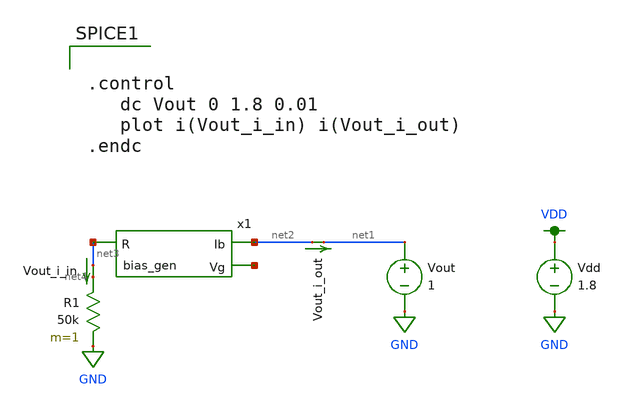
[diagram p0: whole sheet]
** sch_path: test_harness_current_mirror_complex.sch
**.subckt test_harness_current_mirror_complex
Vdd VDD GND 1.8
R1 net4 GND 50k m=1
x1 net2 net5 net3 bias_gen
Vout_i_in net3 net4 0
.save i(vout_i_in)
Vout net1 GND 1
Vout_i_out net2 net1 0
.save i(vout_i_out)
**** begin user architecture code


.control
   dc Vout 0 1.8 0.01
   plot i(Vout_i_in) i(Vout_i_out)
.endc


.option wnflag=1
.param MC_SWITCH=0.0
.lib ~/skywater/skywater-pdk/libraries/sky130_fd_pr_ngspice/latest/models/sky130.lib.spice tt

**** end user architecture code
**.ends

* expanding   symbol:  /home/madvlsi/Documents/R2R-DAC/bias_gen.sym # of pins=3
** sym_path: bias_gen.sym
** sch_path: bias_gen.sch
.subckt bias_gen Ib Vg R
*.ipin R
*.opin Ib
*.opin Vg
XM2 R net2 net2 GND sky130_fd_pr__nfet_01v8 L=4 W=96 nf=1 ad='int((nf+1)/2) * W/nf * 0.29' as='int((nf+2)/2) * W/nf * 0.29'
+ pd='2*int((nf+1)/2) * (W/nf + 0.29)' ps='2*int((nf+2)/2) * (W/nf + 0.29)' nrd='0.29 / W' nrs='0.29 / W'
+ sa=0 sb=0 sd=0 mult=1 m=1
XM3 VDD net1 net1 VDD sky130_fd_pr__pfet_01v8 L=4 W=12 nf=1 ad='int((nf+1)/2) * W/nf * 0.29' as='int((nf+2)/2) * W/nf * 0.29'
+ pd='2*int((nf+1)/2) * (W/nf + 0.29)' ps='2*int((nf+2)/2) * (W/nf + 0.29)' nrd='0.29 / W' nrs='0.29 / W'
+ sa=0 sb=0 sd=0 mult=1 m=1
XM1 VDD Vg net2 VDD sky130_fd_pr__pfet_01v8 L=4 W=12 nf=1 ad='int((nf+1)/2) * W/nf * 0.29' as='int((nf+2)/2) * W/nf * 0.29'
+ pd='2*int((nf+1)/2) * (W/nf + 0.29)' ps='2*int((nf+2)/2) * (W/nf + 0.29)' nrd='0.29 / W' nrs='0.29 / W'
+ sa=0 sb=0 sd=0 mult=1 m=1
XM4 Vg net1 VDD VDD sky130_fd_pr__pfet_01v8 L=4 W=12 nf=1 ad='int((nf+1)/2) * W/nf * 0.29' as='int((nf+2)/2) * W/nf * 0.29'
+ pd='2*int((nf+1)/2) * (W/nf + 0.29)' ps='2*int((nf+2)/2) * (W/nf + 0.29)' nrd='0.29 / W' nrs='0.29 / W'
+ sa=0 sb=0 sd=0 mult=1 m=1
XM5 net3 Vg VDD VDD sky130_fd_pr__pfet_01v8 L=4 W=12 nf=1 ad='int((nf+1)/2) * W/nf * 0.29' as='int((nf+2)/2) * W/nf * 0.29'
+ pd='2*int((nf+1)/2) * (W/nf + 0.29)' ps='2*int((nf+2)/2) * (W/nf + 0.29)' nrd='0.29 / W' nrs='0.29 / W'
+ sa=0 sb=0 sd=0 mult=1 m=1
XM7 Ib Vg VDD VDD sky130_fd_pr__pfet_01v8 L=4 W=12 nf=1 ad='int((nf+1)/2) * W/nf * 0.29' as='int((nf+2)/2) * W/nf * 0.29'
+ pd='2*int((nf+1)/2) * (W/nf + 0.29)' ps='2*int((nf+2)/2) * (W/nf + 0.29)' nrd='0.29 / W' nrs='0.29 / W'
+ sa=0 sb=0 sd=0 mult=1 m=1
XM6 net1 net2 GND GND sky130_fd_pr__nfet_01v8 L=4 W=12 nf=1 ad='int((nf+1)/2) * W/nf * 0.29' as='int((nf+2)/2) * W/nf * 0.29'
+ pd='2*int((nf+1)/2) * (W/nf + 0.29)' ps='2*int((nf+2)/2) * (W/nf + 0.29)' nrd='0.29 / W' nrs='0.29 / W'
+ sa=0 sb=0 sd=0 mult=1 m=1
XM8 GND net3 Vg GND sky130_fd_pr__nfet_01v8 L=4 W=12 nf=1 ad='int((nf+1)/2) * W/nf * 0.29' as='int((nf+2)/2) * W/nf * 0.29'
+ pd='2*int((nf+1)/2) * (W/nf + 0.29)' ps='2*int((nf+2)/2) * (W/nf + 0.29)' nrd='0.29 / W' nrs='0.29 / W'
+ sa=0 sb=0 sd=0 mult=1 m=1
XM9 net3 net3 GND GND sky130_fd_pr__nfet_01v8 L=4 W=12 nf=1 ad='int((nf+1)/2) * W/nf * 0.29' as='int((nf+2)/2) * W/nf * 0.29'
+ pd='2*int((nf+1)/2) * (W/nf + 0.29)' ps='2*int((nf+2)/2) * (W/nf + 0.29)' nrd='0.29 / W' nrs='0.29 / W'
+ sa=0 sb=0 sd=0 mult=1 m=1
.ends

.GLOBAL GND
.GLOBAL VDD
.end
